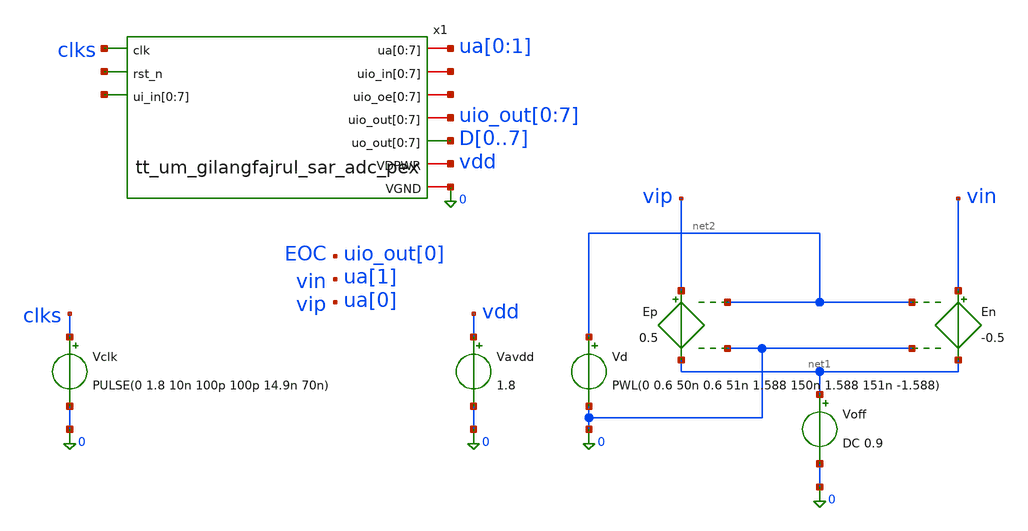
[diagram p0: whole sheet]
** sch_path: xschem/sar-adc_tb/sar-adc-pex_tb.sch
.lib $::SKYWATER_MODELS/sky130.lib.spice tt
.include $::SKYWATER_STDCELLS/sky130_fd_sc_hd.spice

**.subckt sar-adc-pex_tb
Vclk clks 0 PULSE(0 1.8 10n 100p 100p 14.9n 70n)
.save i(vclk)
Vavdd vdd 0 1.8
.save i(vavdd)
Voff net1 0 DC 0.9
.save i(voff)
En vin net1 net2 0 -0.5
Ep vip net1 net2 0 0.5
Vd net2 0 PWL(0 0.6 50n 0.6 51n 1.588 150n 1.588 151n -1.588)
.save i(vd)
x1 clks net3 ua[0] ua[1] ua[0] ua[1] ua[0] ua[1] ua[0] ua[1] net4[7] net4[6] net4[5] net4[4] net4[3]
+ net4[2] net4[1] net4[0] net5[7] net5[6] net5[5] net5[4] net5[3] net5[2] net5[1] net5[0] net6[7] net6[6]
+ net6[5] net6[4] net6[3] net6[2] net6[1] net6[0] uio_out[0] uio_out[1] uio_out[2] uio_out[3] uio_out[4]
+ uio_out[5] uio_out[6] uio_out[7] D0 D1 D2 D3 D4 D5 D6 D7 vdd 0 tt_um_gilangfajrul_sar_adc_pex
**** begin user architecture code



.include /foss/designs/ttsky26c-saradc/pex/tt_um_gilangfajrul_sar_adc.pex.spice
.control
 remzerovec
 save v(clks) v(EOC) v(vip) v(vin) v(xtop.d7) v(xtop.d6) v(xtop.d5) v(xtop.d4) v(xtop.d3) v(xtop.d2)
+ v(xtop.d1) v(xtop.d0) v(xtop.ctopp) v(xtop.ctopn) v(xtop.clkc) v(xtop.comp_valid) v(xtop.comp_vop)
+ v(xtop.comp_von) v(xtop.clk1) v(xtop.clk2) v(xtop.clk3) v(xtop.clk4) v(xtop.clk5) v(xtop.clk6) v(xtop.clk7)
+ v(xtop.clk8) v(xtop.xcomparator.vtail)
 + v(xtop.xcomparator.pcp) v(xtop.xcomparator.pcn)
 + v(d7) v(d6) v(d5) v(d4) v(d3) v(d2) v(d1) v(d0)
 tran 20p 350n
 write sar-adc_tb.raw
.endc





.param nfft = 64
.param mcyc = 29
.param fs = 10e6
.param fin  = 'mcyc/nfft*fs'     $ 4.53125 MHz
.param amp  = 0.88               $ hampir full-scale single-ended
.param off  = 0.9                $ V_CM
.param namp = '-amp'             $ amplitudo sisi n (fase berlawanan)
.options reltol=1e-4 vntol=1e-8 abstol=1e-14 chgtol=1e-16


**** end user architecture code
**.ends

* expanding   symbol:  tt_um_gilangfajrul_sar_adc_pex.sym # of pins=10
** sym_path: xschem/sar-adc/tt_um_gilangfajrul_sar_adc_pex.sym
** sch_path: xschem/sar-adc/tt_um_gilangfajrul_sar_adc_pex.sch
.subckt tt_um_gilangfajrul_sar_adc_pex clk rst_n ua[0] ua[1] ua[2] ua[3] ua[4] ua[5] ua[6] ua[7]
+ ui_in[0] ui_in[1] ui_in[2] ui_in[3] ui_in[4] ui_in[5] ui_in[6] ui_in[7] uio_in[0] uio_in[1] uio_in[2]
+ uio_in[3] uio_in[4] uio_in[5] uio_in[6] uio_in[7] uio_oe[0] uio_oe[1] uio_oe[2] uio_oe[3] uio_oe[4] uio_oe[5]
+ uio_oe[6] uio_oe[7] uio_out[0] uio_out[1] uio_out[2] uio_out[3] uio_out[4] uio_out[5] uio_out[6] uio_out[7]
+ uo_out[0] uo_out[1] uo_out[2] uo_out[3] uo_out[4] uo_out[5] uo_out[6] uo_out[7] VDPWR VGND
*.ipin clk
*.ipin rst_n
*.iopin ua[0],ua[1],ua[2],ua[3],ua[4],ua[5],ua[6],ua[7]
*.ipin ui_in[0],ui_in[1],ui_in[2],ui_in[3],ui_in[4],ui_in[5],ui_in[6],ui_in[7]
*.iopin uio_in[0],uio_in[1],uio_in[2],uio_in[3],uio_in[4],uio_in[5],uio_in[6],uio_in[7]
*.iopin uio_oe[0],uio_oe[1],uio_oe[2],uio_oe[3],uio_oe[4],uio_oe[5],uio_oe[6],uio_oe[7]
*.iopin uio_out[0],uio_out[1],uio_out[2],uio_out[3],uio_out[4],uio_out[5],uio_out[6],uio_out[7]
*.opin uo_out[0],uo_out[1],uo_out[2],uo_out[3],uo_out[4],uo_out[5],uo_out[6],uo_out[7]
*.iopin VDPWR
*.iopin VGND
.ends

.end
